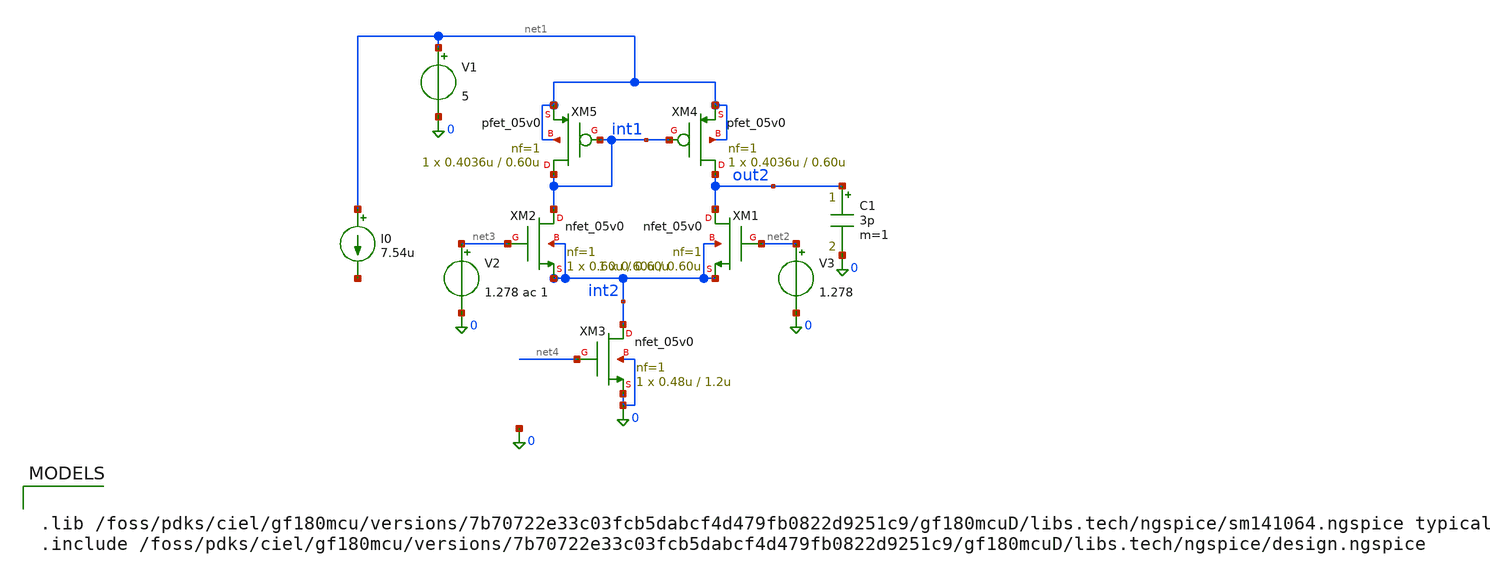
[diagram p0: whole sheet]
** sch_path: schema_ram/1_OTA.sch
**.subckt 1_OTA
XM1 out2 net2 int2 int2 nfet_05v0 L=0.60u W=0.60u nf=1 ad='int((nf+1)/2) * W/nf * 0.18u' as='int((nf+2)/2) * W/nf * 0.18u'
+ pd='2*int((nf+1)/2) * (W/nf + 0.18u)' ps='2*int((nf+2)/2) * (W/nf + 0.18u)' nrd='0.18u / W' nrs='0.18u / W'
+ sa=0 sb=0 sd=0 m=1
XM2 int1 net3 int2 int2 nfet_05v0 L=0.60u W=0.60u nf=1 ad='int((nf+1)/2) * W/nf * 0.18u' as='int((nf+2)/2) * W/nf * 0.18u'
+ pd='2*int((nf+1)/2) * (W/nf + 0.18u)' ps='2*int((nf+2)/2) * (W/nf + 0.18u)' nrd='0.18u / W' nrs='0.18u / W'
+ sa=0 sb=0 sd=0 m=1
XM3 int2 net4 0 0 nfet_05v0 L=1.2u W=0.48u nf=1 ad='int((nf+1)/2) * W/nf * 0.18u' as='int((nf+2)/2) * W/nf * 0.18u'
+ pd='2*int((nf+1)/2) * (W/nf + 0.18u)' ps='2*int((nf+2)/2) * (W/nf + 0.18u)' nrd='0.18u / W' nrs='0.18u / W'
+ sa=0 sb=0 sd=0 m=1
XM4 out2 int1 net1 net1 pfet_05v0 L=0.60u W=0.4036u nf=1 ad='int((nf+1)/2) * W/nf * 0.18u' as='int((nf+2)/2) * W/nf * 0.18u'
+ pd='2*int((nf+1)/2) * (W/nf + 0.18u)' ps='2*int((nf+2)/2) * (W/nf + 0.18u)' nrd='0.18u / W' nrs='0.18u / W'
+ sa=0 sb=0 sd=0 m=1
XM5 int1 int1 net1 net1 pfet_05v0 L=0.60u W=0.4036u nf=1 ad='int((nf+1)/2) * W/nf * 0.18u' as='int((nf+2)/2) * W/nf * 0.18u'
+ pd='2*int((nf+1)/2) * (W/nf + 0.18u)' ps='2*int((nf+2)/2) * (W/nf + 0.18u)' nrd='0.18u / W' nrs='0.18u / W'
+ sa=0 sb=0 sd=0 m=1
V1 net1 0 5
V2 net3 0 1.278 ac 1
V3 net2 0 1.278
C1 out2 0 3p m=1
I0 net1 net5 7.54u
**** begin user architecture code


.lib /foss/pdks/ciel/gf180mcu/versions/7b70722e33c03fcb5dabcf4d479fb0822d9251c9/gf180mcuD/libs.tech/ngspice/sm141064.ngspice typical
.include /foss/pdks/ciel/gf180mcu/versions/7b70722e33c03fcb5dabcf4d479fb0822d9251c9/gf180mcuD/libs.tech/ngspice/design.ngspice




.control
  	save all
	op
	#ac dec 20 1 100Meg
	remzerovec
	write 1_OTA_ac.raw
.endc

.options savecurrents


**** end user architecture code
**.ends
.end
